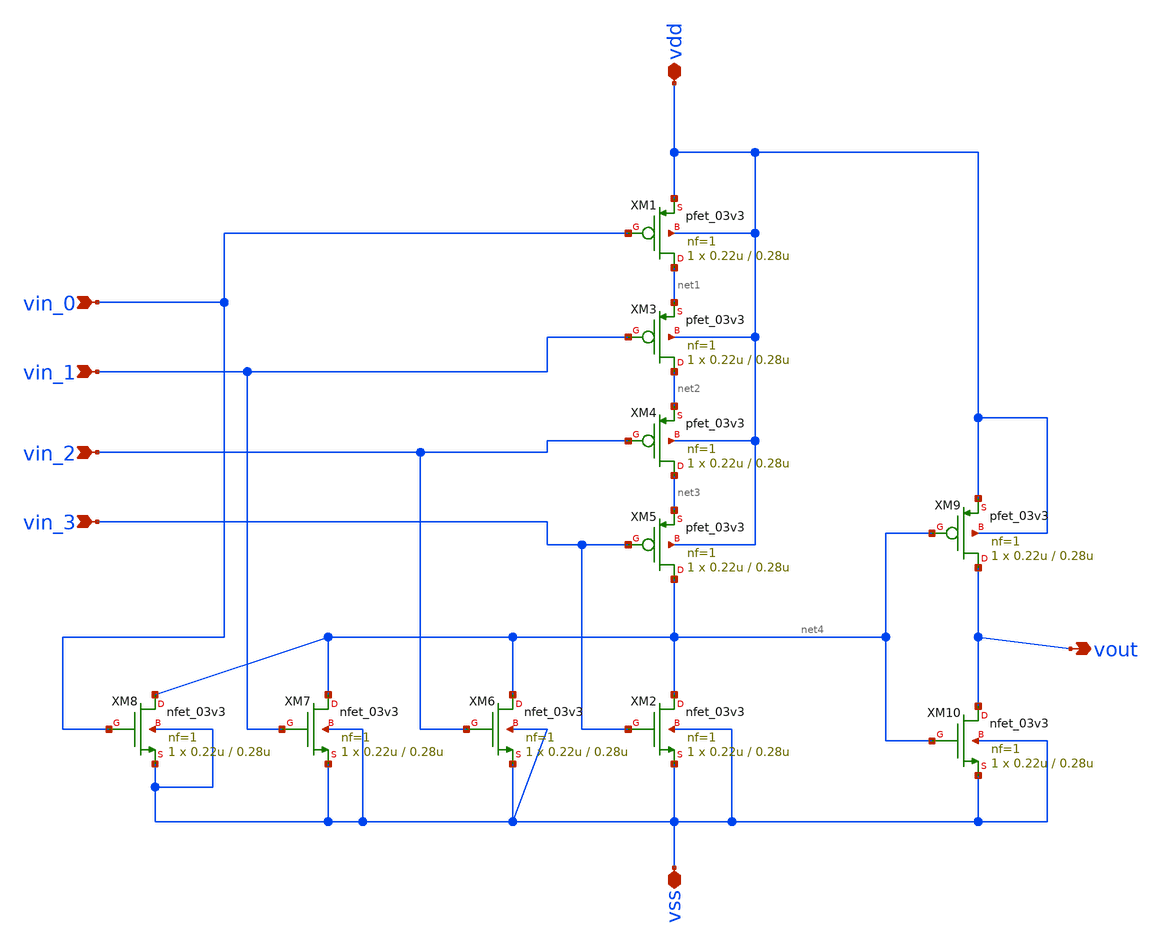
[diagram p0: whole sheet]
** sch_path: designs/4_input_or.sch
**.subckt 4_input_or vdd vss vin_0 vin_1 vin_2 vin_3 vout
*.iopin vdd
*.iopin vss
*.ipin vin_0
*.ipin vin_1
*.ipin vin_2
*.ipin vin_3
*.opin vout
XM1 net1 vin_0 vdd vdd pfet_03v3 L=0.28u W=0.22u nf=1 ad='int((nf+1)/2) * W/nf * 0.18u' as='int((nf+2)/2) * W/nf * 0.18u'
+ pd='2*int((nf+1)/2) * (W/nf + 0.18u)' ps='2*int((nf+2)/2) * (W/nf + 0.18u)' nrd='0.18u / W' nrs='0.18u / W'
+ sa=0 sb=0 sd=0 m=1
XM2 net4 vin_3 vss vss nfet_03v3 L=0.28u W=0.22u nf=1 ad='int((nf+1)/2) * W/nf * 0.18u' as='int((nf+2)/2) * W/nf * 0.18u'
+ pd='2*int((nf+1)/2) * (W/nf + 0.18u)' ps='2*int((nf+2)/2) * (W/nf + 0.18u)' nrd='0.18u / W' nrs='0.18u / W'
+ sa=0 sb=0 sd=0 m=1
XM3 net2 vin_1 net1 vdd pfet_03v3 L=0.28u W=0.22u nf=1 ad='int((nf+1)/2) * W/nf * 0.18u' as='int((nf+2)/2) * W/nf * 0.18u'
+ pd='2*int((nf+1)/2) * (W/nf + 0.18u)' ps='2*int((nf+2)/2) * (W/nf + 0.18u)' nrd='0.18u / W' nrs='0.18u / W'
+ sa=0 sb=0 sd=0 m=1
XM4 net3 vin_2 net2 vdd pfet_03v3 L=0.28u W=0.22u nf=1 ad='int((nf+1)/2) * W/nf * 0.18u' as='int((nf+2)/2) * W/nf * 0.18u'
+ pd='2*int((nf+1)/2) * (W/nf + 0.18u)' ps='2*int((nf+2)/2) * (W/nf + 0.18u)' nrd='0.18u / W' nrs='0.18u / W'
+ sa=0 sb=0 sd=0 m=1
XM5 net4 vin_3 net3 vdd pfet_03v3 L=0.28u W=0.22u nf=1 ad='int((nf+1)/2) * W/nf * 0.18u' as='int((nf+2)/2) * W/nf * 0.18u'
+ pd='2*int((nf+1)/2) * (W/nf + 0.18u)' ps='2*int((nf+2)/2) * (W/nf + 0.18u)' nrd='0.18u / W' nrs='0.18u / W'
+ sa=0 sb=0 sd=0 m=1
XM6 net4 vin_2 vss vss nfet_03v3 L=0.28u W=0.22u nf=1 ad='int((nf+1)/2) * W/nf * 0.18u' as='int((nf+2)/2) * W/nf * 0.18u'
+ pd='2*int((nf+1)/2) * (W/nf + 0.18u)' ps='2*int((nf+2)/2) * (W/nf + 0.18u)' nrd='0.18u / W' nrs='0.18u / W'
+ sa=0 sb=0 sd=0 m=1
XM7 net4 vin_1 vss vss nfet_03v3 L=0.28u W=0.22u nf=1 ad='int((nf+1)/2) * W/nf * 0.18u' as='int((nf+2)/2) * W/nf * 0.18u'
+ pd='2*int((nf+1)/2) * (W/nf + 0.18u)' ps='2*int((nf+2)/2) * (W/nf + 0.18u)' nrd='0.18u / W' nrs='0.18u / W'
+ sa=0 sb=0 sd=0 m=1
XM8 net4 vin_0 vss vss nfet_03v3 L=0.28u W=0.22u nf=1 ad='int((nf+1)/2) * W/nf * 0.18u' as='int((nf+2)/2) * W/nf * 0.18u'
+ pd='2*int((nf+1)/2) * (W/nf + 0.18u)' ps='2*int((nf+2)/2) * (W/nf + 0.18u)' nrd='0.18u / W' nrs='0.18u / W'
+ sa=0 sb=0 sd=0 m=1
XM9 vout net4 vdd vdd pfet_03v3 L=0.28u W=0.22u nf=1 ad='int((nf+1)/2) * W/nf * 0.18u' as='int((nf+2)/2) * W/nf * 0.18u'
+ pd='2*int((nf+1)/2) * (W/nf + 0.18u)' ps='2*int((nf+2)/2) * (W/nf + 0.18u)' nrd='0.18u / W' nrs='0.18u / W'
+ sa=0 sb=0 sd=0 m=1
XM10 vout net4 vss vss nfet_03v3 L=0.28u W=0.22u nf=1 ad='int((nf+1)/2) * W/nf * 0.18u' as='int((nf+2)/2) * W/nf * 0.18u'
+ pd='2*int((nf+1)/2) * (W/nf + 0.18u)' ps='2*int((nf+2)/2) * (W/nf + 0.18u)' nrd='0.18u / W' nrs='0.18u / W'
+ sa=0 sb=0 sd=0 m=1
**.ends
.end
